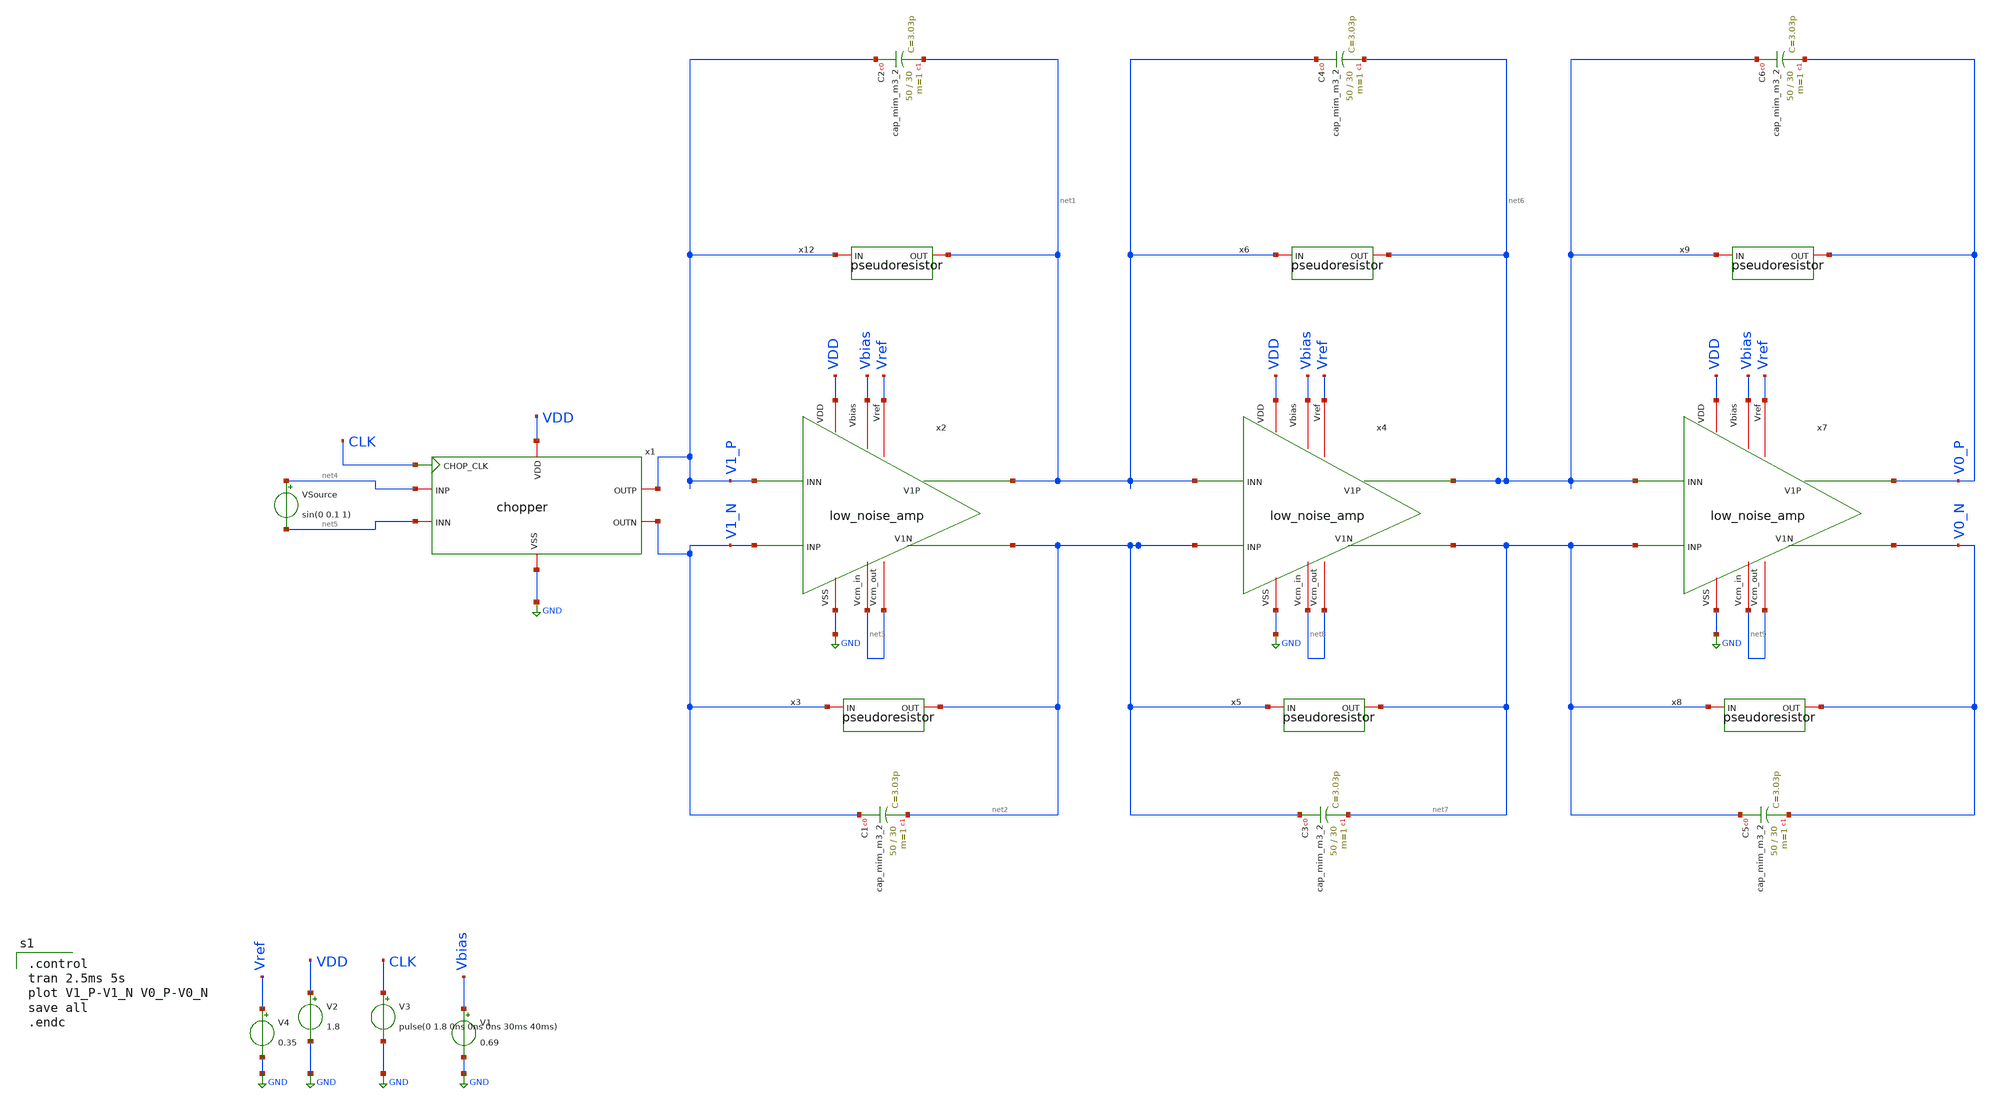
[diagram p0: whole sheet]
** sch_path: opamp_lna/chopper_LNA_tb.sch
**.subckt chopper_LNA_tb
VSource net4 net5 sin(0 0.1 1)
V2 VDD GND 1.8
V3 CLK GND pulse(0 1.8 0ns 0ns 0ns 30ms 40ms)
V1 Vbias GND 0.69
V4 Vref GND 0.35
x2 VDD net3 V1_P V1_N net1 net2 GND net3 Vbias Vref low_noise_amp
x3 V1_N net2 pseudoresistor
XC1 V1_N net2 sky130_fd_pr__cap_mim_m3_2 W=50 L=30 MF=1 m=1
XC2 V1_P net1 sky130_fd_pr__cap_mim_m3_2 W=50 L=30 MF=1 m=1
x12 V1_P net1 pseudoresistor
x1 GND VDD V1_P net4 CLK V1_N net5 chopper
x4 VDD net8 net1 net2 net6 net7 GND net8 Vbias Vref low_noise_amp
x5 net2 net7 pseudoresistor
XC3 net2 net7 sky130_fd_pr__cap_mim_m3_2 W=50 L=30 MF=1 m=1
XC4 net1 net6 sky130_fd_pr__cap_mim_m3_2 W=50 L=30 MF=1 m=1
x6 net1 net6 pseudoresistor
x7 VDD net9 net6 net7 V0_P V0_N GND net9 Vbias Vref low_noise_amp
x8 net7 V0_N pseudoresistor
XC5 net7 V0_N sky130_fd_pr__cap_mim_m3_2 W=50 L=30 MF=1 m=1
XC6 net6 V0_P sky130_fd_pr__cap_mim_m3_2 W=50 L=30 MF=1 m=1
x9 net6 V0_P pseudoresistor
**** begin user architecture code

.control
tran 2.5ms 5s
plot V1_P-V1_N V0_P-V0_N
save all
.endc


** opencircuitdesign pdks install
.lib $::SKYWATER_MODELS/sky130.lib.spice tt
.include $::SKYWATER_STDCELLS/sky130_fd_sc_hd.spice

**** end user architecture code
**.ends

* expanding   symbol:  low_noise_amp.sym # of pins=10
** sym_path: opamp_lna/low_noise_amp.sym
** sch_path: opamp_lna/low_noise_amp.sch
.subckt low_noise_amp VDD Vcm_in INN INP V1P V1N VSS Vcm_out Vbias Vref
*.iopin VDD
*.iopin VSS
*.iopin Vbias
*.ipin INP
*.ipin INN
*.iopin Vref
*.iopin Vcm_in
*.iopin Vcm_out
*.opin V1N
*.opin V1P
XM3 CMFB Vref A0 VDD sky130_fd_pr__pfet_01v8 L=0.8 W=8 nf=1 ad='int((nf+1)/2) * W/nf * 0.29' as='int((nf+2)/2) * W/nf * 0.29'
+ pd='2*int((nf+1)/2) * (W/nf + 0.29)' ps='2*int((nf+2)/2) * (W/nf + 0.29)' nrd='0.29 / W' nrs='0.29 / W'
+ sa=0 sb=0 sd=0 mult=1 m=1
XM11 A0 Vbias VDD VDD sky130_fd_pr__pfet_01v8 L=0.8 W=4 nf=1 ad='int((nf+1)/2) * W/nf * 0.29' as='int((nf+2)/2) * W/nf * 0.29'
+ pd='2*int((nf+1)/2) * (W/nf + 0.29)' ps='2*int((nf+2)/2) * (W/nf + 0.29)' nrd='0.29 / W' nrs='0.29 / W'
+ sa=0 sb=0 sd=0 mult=1 m=1
XM7 V1N INP B0 VDD sky130_fd_pr__pfet_01v8 L=2 W=18 nf=1 ad='int((nf+1)/2) * W/nf * 0.29' as='int((nf+2)/2) * W/nf * 0.29'
+ pd='2*int((nf+1)/2) * (W/nf + 0.29)' ps='2*int((nf+2)/2) * (W/nf + 0.29)' nrd='0.29 / W' nrs='0.29 / W'
+ sa=0 sb=0 sd=0 mult=1 m=1
XM8 V1P INN B0 VDD sky130_fd_pr__pfet_01v8 L=2 W=18 nf=1 ad='int((nf+1)/2) * W/nf * 0.29' as='int((nf+2)/2) * W/nf * 0.29'
+ pd='2*int((nf+1)/2) * (W/nf + 0.29)' ps='2*int((nf+2)/2) * (W/nf + 0.29)' nrd='0.29 / W' nrs='0.29 / W'
+ sa=0 sb=0 sd=0 mult=1 m=1
XM9 V1N INP B1 VSS sky130_fd_pr__nfet_01v8 L=1 W=12 nf=1 ad='int((nf+1)/2) * W/nf * 0.29' as='int((nf+2)/2) * W/nf * 0.29'
+ pd='2*int((nf+1)/2) * (W/nf + 0.29)' ps='2*int((nf+2)/2) * (W/nf + 0.29)' nrd='0.29 / W' nrs='0.29 / W'
+ sa=0 sb=0 sd=0 mult=1 m=1
XM12 B0 Vbias VDD VDD sky130_fd_pr__pfet_01v8 L=0.8 W=4 nf=1 ad='int((nf+1)/2) * W/nf * 0.29' as='int((nf+2)/2) * W/nf * 0.29'
+ pd='2*int((nf+1)/2) * (W/nf + 0.29)' ps='2*int((nf+2)/2) * (W/nf + 0.29)' nrd='0.29 / W' nrs='0.29 / W'
+ sa=0 sb=0 sd=0 mult=1 m=1
XM13 B1 CMFB VSS VSS sky130_fd_pr__nfet_01v8 L=0.8 W=2 nf=1 ad='int((nf+1)/2) * W/nf * 0.29' as='int((nf+2)/2) * W/nf * 0.29'
+ pd='2*int((nf+1)/2) * (W/nf + 0.29)' ps='2*int((nf+2)/2) * (W/nf + 0.29)' nrd='0.29 / W' nrs='0.29 / W'
+ sa=0 sb=0 sd=0 mult=1 m=1
XM15 Vcm_out Vcm_out net1 Vcm_out sky130_fd_pr__pfet_01v8 L=0.6 W=1 nf=1 ad='int((nf+1)/2) * W/nf * 0.29'
+ as='int((nf+2)/2) * W/nf * 0.29' pd='2*int((nf+1)/2) * (W/nf + 0.29)' ps='2*int((nf+2)/2) * (W/nf + 0.29)'
+ nrd='0.29 / W' nrs='0.29 / W' sa=0 sb=0 sd=0 mult=5 m=5
XM16 net1 V1P V1P V1P sky130_fd_pr__pfet_01v8 L=0.6 W=1 nf=1 ad='int((nf+1)/2) * W/nf * 0.29' as='int((nf+2)/2) * W/nf * 0.29'
+ pd='2*int((nf+1)/2) * (W/nf + 0.29)' ps='2*int((nf+2)/2) * (W/nf + 0.29)' nrd='0.29 / W' nrs='0.29 / W'
+ sa=0 sb=0 sd=0 mult=5 m=5
XM17 Vcm_out Vcm_out net2 Vcm_out sky130_fd_pr__pfet_01v8 L=0.6 W=1 nf=1 ad='int((nf+1)/2) * W/nf * 0.29'
+ as='int((nf+2)/2) * W/nf * 0.29' pd='2*int((nf+1)/2) * (W/nf + 0.29)' ps='2*int((nf+2)/2) * (W/nf + 0.29)'
+ nrd='0.29 / W' nrs='0.29 / W' sa=0 sb=0 sd=0 mult=5 m=5
XM18 net2 V1N V1N V1N sky130_fd_pr__pfet_01v8 L=0.6 W=1 nf=1 ad='int((nf+1)/2) * W/nf * 0.29' as='int((nf+2)/2) * W/nf * 0.29'
+ pd='2*int((nf+1)/2) * (W/nf + 0.29)' ps='2*int((nf+2)/2) * (W/nf + 0.29)' nrd='0.29 / W' nrs='0.29 / W'
+ sa=0 sb=0 sd=0 mult=5 m=5
XC1 Vcm_out VSS sky130_fd_pr__cap_mim_m3_1 W=1 L=1 MF=1 m=1
XM1 V1P INN B1 VSS sky130_fd_pr__nfet_01v8 L=1 W=12 nf=1 ad='int((nf+1)/2) * W/nf * 0.29' as='int((nf+2)/2) * W/nf * 0.29'
+ pd='2*int((nf+1)/2) * (W/nf + 0.29)' ps='2*int((nf+2)/2) * (W/nf + 0.29)' nrd='0.29 / W' nrs='0.29 / W'
+ sa=0 sb=0 sd=0 mult=1 m=1
XM2 A1 A1 VSS VSS sky130_fd_pr__nfet_01v8 L=0.8 W=6 nf=1 ad='int((nf+1)/2) * W/nf * 0.29' as='int((nf+2)/2) * W/nf * 0.29'
+ pd='2*int((nf+1)/2) * (W/nf + 0.29)' ps='2*int((nf+2)/2) * (W/nf + 0.29)' nrd='0.29 / W' nrs='0.29 / W'
+ sa=0 sb=0 sd=0 mult=1 m=1
XM5 CMFB A1 VSS VSS sky130_fd_pr__nfet_01v8 L=0.8 W=6 nf=1 ad='int((nf+1)/2) * W/nf * 0.29' as='int((nf+2)/2) * W/nf * 0.29'
+ pd='2*int((nf+1)/2) * (W/nf + 0.29)' ps='2*int((nf+2)/2) * (W/nf + 0.29)' nrd='0.29 / W' nrs='0.29 / W'
+ sa=0 sb=0 sd=0 mult=1 m=1
XM6 A1 Vcm_in A0 VDD sky130_fd_pr__pfet_01v8 L=0.8 W=8 nf=1 ad='int((nf+1)/2) * W/nf * 0.29' as='int((nf+2)/2) * W/nf * 0.29'
+ pd='2*int((nf+1)/2) * (W/nf + 0.29)' ps='2*int((nf+2)/2) * (W/nf + 0.29)' nrd='0.29 / W' nrs='0.29 / W'
+ sa=0 sb=0 sd=0 mult=1 m=1
.ends


* expanding   symbol:  /home/lcg3895/CE393/pseudoresistor.sym # of pins=2
** sym_path: opamp_lna/pseudoresistor.sym
** sch_path: opamp_lna/pseudoresistor.sch
.subckt pseudoresistor IN OUT
*.iopin IN
*.iopin OUT
XM5 net1 IN IN IN sky130_fd_pr__pfet_01v8 L=0.5 W=1 nf=5 ad='int((nf+1)/2) * W/nf * 0.29' as='int((nf+2)/2) * W/nf * 0.29'
+ pd='2*int((nf+1)/2) * (W/nf + 0.29)' ps='2*int((nf+2)/2) * (W/nf + 0.29)' nrd='0.29 / W' nrs='0.29 / W'
+ sa=0 sb=0 sd=0 mult=1 m=1
XM1 net2 net2 net1 net2 sky130_fd_pr__pfet_01v8 L=0.5 W=1 nf=5 ad='int((nf+1)/2) * W/nf * 0.29' as='int((nf+2)/2) * W/nf * 0.29'
+ pd='2*int((nf+1)/2) * (W/nf + 0.29)' ps='2*int((nf+2)/2) * (W/nf + 0.29)' nrd='0.29 / W' nrs='0.29 / W'
+ sa=0 sb=0 sd=0 mult=1 m=1
XM2 net3 net2 net2 net2 sky130_fd_pr__pfet_01v8 L=0.5 W=1 nf=5 ad='int((nf+1)/2) * W/nf * 0.29' as='int((nf+2)/2) * W/nf * 0.29'
+ pd='2*int((nf+1)/2) * (W/nf + 0.29)' ps='2*int((nf+2)/2) * (W/nf + 0.29)' nrd='0.29 / W' nrs='0.29 / W'
+ sa=0 sb=0 sd=0 mult=1 m=1
XM3 OUT OUT net3 OUT sky130_fd_pr__pfet_01v8 L=0.5 W=1 nf=5 ad='int((nf+1)/2) * W/nf * 0.29' as='int((nf+2)/2) * W/nf * 0.29'
+ pd='2*int((nf+1)/2) * (W/nf + 0.29)' ps='2*int((nf+2)/2) * (W/nf + 0.29)' nrd='0.29 / W' nrs='0.29 / W'
+ sa=0 sb=0 sd=0 mult=1 m=1
.ends


* expanding   symbol:  chopper.sym # of pins=7
** sym_path: opamp_lna/chopper.sym
** sch_path: opamp_lna/chopper.sch
.subckt chopper VSS VDD OUTP INP CHOP_CLK OUTN INN
*.ipin CHOP_CLK
*.iopin INP
*.iopin INN
*.iopin OUTP
*.iopin OUTN
*.iopin VSS
*.iopin VDD
x5 CHOP_CLK VSS VNB VPB VDD net2 sky130_fd_sc_hd__clkbuf_2
x1 CHOP_CLK VGND VNB VPB VPWR net1 sky130_fd_sc_hd__clkinv_2
x2 net1 VSS VNB VPB VDD SWB sky130_fd_sc_hd__clkinv_8
x3 net2 VSS VNB VPB VDD SW sky130_fd_sc_hd__clkinv_8
XM5 INP SWB OUTN VSS sky130_fd_pr__nfet_01v8 L=0.15 W=1 nf=1 ad='int((nf+1)/2) * W/nf * 0.29' as='int((nf+2)/2) * W/nf * 0.29'
+ pd='2*int((nf+1)/2) * (W/nf + 0.29)' ps='2*int((nf+2)/2) * (W/nf + 0.29)' nrd='0.29 / W' nrs='0.29 / W'
+ sa=0 sb=0 sd=0 mult=1 m=1
XM6 OUTN SW INP VDD sky130_fd_pr__pfet_01v8 L=0.15 W=1 nf=1 ad='int((nf+1)/2) * W/nf * 0.29' as='int((nf+2)/2) * W/nf * 0.29'
+ pd='2*int((nf+1)/2) * (W/nf + 0.29)' ps='2*int((nf+2)/2) * (W/nf + 0.29)' nrd='0.29 / W' nrs='0.29 / W'
+ sa=0 sb=0 sd=0 mult=1 m=1
XM7 INP SW OUTP VSS sky130_fd_pr__nfet_01v8 L=0.15 W=8 nf=1 ad='int((nf+1)/2) * W/nf * 0.29' as='int((nf+2)/2) * W/nf * 0.29'
+ pd='2*int((nf+1)/2) * (W/nf + 0.29)' ps='2*int((nf+2)/2) * (W/nf + 0.29)' nrd='0.29 / W' nrs='0.29 / W'
+ sa=0 sb=0 sd=0 mult=1 m=1
XM8 OUTP SWB INP VDD sky130_fd_pr__pfet_01v8 L=0.15 W=8 nf=1 ad='int((nf+1)/2) * W/nf * 0.29' as='int((nf+2)/2) * W/nf * 0.29'
+ pd='2*int((nf+1)/2) * (W/nf + 0.29)' ps='2*int((nf+2)/2) * (W/nf + 0.29)' nrd='0.29 / W' nrs='0.29 / W'
+ sa=0 sb=0 sd=0 mult=1 m=1
XM9 INN SW OUTN VSS sky130_fd_pr__nfet_01v8 L=0.15 W=8 nf=1 ad='int((nf+1)/2) * W/nf * 0.29' as='int((nf+2)/2) * W/nf * 0.29'
+ pd='2*int((nf+1)/2) * (W/nf + 0.29)' ps='2*int((nf+2)/2) * (W/nf + 0.29)' nrd='0.29 / W' nrs='0.29 / W'
+ sa=0 sb=0 sd=0 mult=1 m=1
XM10 OUTN SWB INN VDD sky130_fd_pr__pfet_01v8 L=0.15 W=8 nf=1 ad='int((nf+1)/2) * W/nf * 0.29' as='int((nf+2)/2) * W/nf * 0.29'
+ pd='2*int((nf+1)/2) * (W/nf + 0.29)' ps='2*int((nf+2)/2) * (W/nf + 0.29)' nrd='0.29 / W' nrs='0.29 / W'
+ sa=0 sb=0 sd=0 mult=1 m=1
XM11 INN SWB OUTP VSS sky130_fd_pr__nfet_01v8 L=0.15 W=8 nf=1 ad='int((nf+1)/2) * W/nf * 0.29' as='int((nf+2)/2) * W/nf * 0.29'
+ pd='2*int((nf+1)/2) * (W/nf + 0.29)' ps='2*int((nf+2)/2) * (W/nf + 0.29)' nrd='0.29 / W' nrs='0.29 / W'
+ sa=0 sb=0 sd=0 mult=1 m=1
XM12 OUTP SW INN VDD sky130_fd_pr__pfet_01v8 L=0.15 W=8 nf=1 ad='int((nf+1)/2) * W/nf * 0.29' as='int((nf+2)/2) * W/nf * 0.29'
+ pd='2*int((nf+1)/2) * (W/nf + 0.29)' ps='2*int((nf+2)/2) * (W/nf + 0.29)' nrd='0.29 / W' nrs='0.29 / W'
+ sa=0 sb=0 sd=0 mult=1 m=1
.ends

.GLOBAL GND
.end
